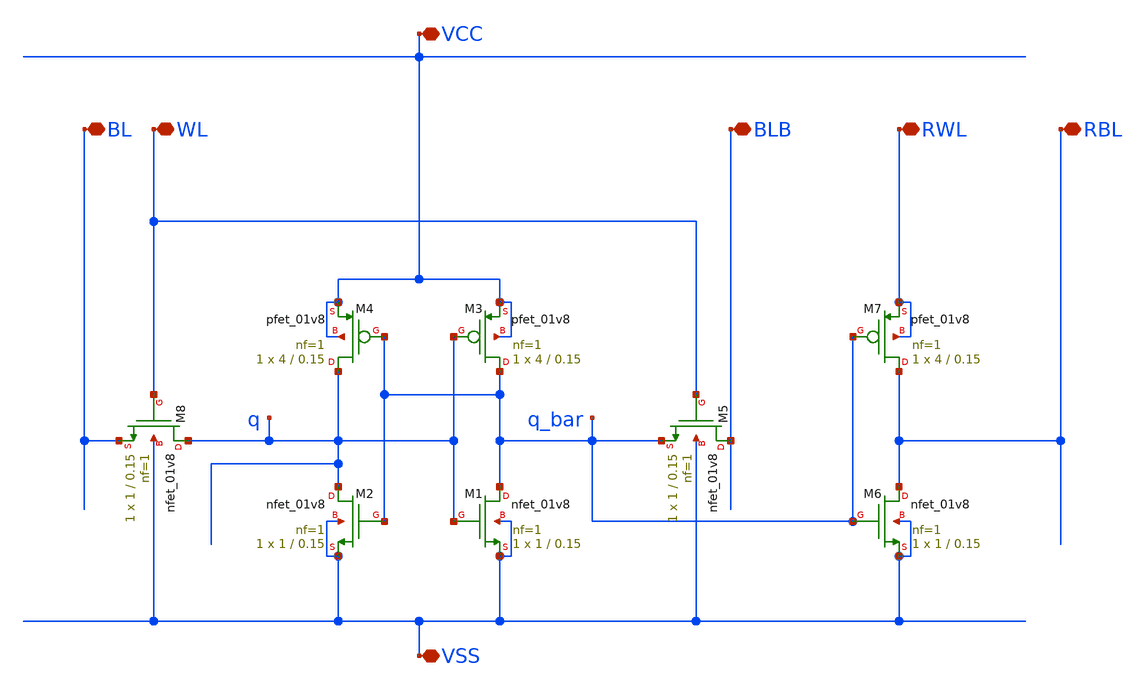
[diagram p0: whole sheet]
** sch_path: 8T_sram_cell2.sch
**.subckt 8T_sram_cell2 VCC BLB WL BL VSS RBL RWL
*.iopin VCC
*.iopin BLB
*.iopin WL
*.iopin BL
*.iopin VSS
*.iopin RBL
*.iopin RWL
XM1 q_bar q VSS VSS sky130_fd_pr__nfet_01v8 L=0.15 W=1 nf=1 ad='int((1 + 1)/2) * 1 / 1 * 0.29' as='int((1 + 2)/2) * 1 / 1 * 0.29'
+ pd='2*int((1 + 1)/2) * (1 / 1 + 0.29)' ps='2*int((1 + 2)/2) * (1 / 1 + 0.29)' nrd='0.29 / 1 ' nrs='0.29 / 1 '
+ sa=0 sb=0 sd=0 mult=1 m=1
XM2 q q_bar VSS VSS sky130_fd_pr__nfet_01v8 L=0.15 W=1 nf=1 ad='int((1 + 1)/2) * 1 / 1 * 0.29' as='int((1 + 2)/2) * 1 / 1 * 0.29'
+ pd='2*int((1 + 1)/2) * (1 / 1 + 0.29)' ps='2*int((1 + 2)/2) * (1 / 1 + 0.29)' nrd='0.29 / 1 ' nrs='0.29 / 1 '
+ sa=0 sb=0 sd=0 mult=1 m=1
XM3 q_bar q VCC VCC sky130_fd_pr__pfet_01v8 L=0.15 W=4 nf=1 ad='int((1 + 1)/2) * 4 / 1 * 0.29' as='int((1 + 2)/2) * 4 / 1 * 0.29'
+ pd='2*int((1 + 1)/2) * (4 / 1 + 0.29)' ps='2*int((1 + 2)/2) * (4 / 1 + 0.29)' nrd='0.29 / 4 ' nrs='0.29 / 4 '
+ sa=0 sb=0 sd=0 mult=1 m=1
XM4 q q_bar VCC VCC sky130_fd_pr__pfet_01v8 L=0.15 W=4 nf=1 ad='int((1 + 1)/2) * 4 / 1 * 0.29' as='int((1 + 2)/2) * 4 / 1 * 0.29'
+ pd='2*int((1 + 1)/2) * (4 / 1 + 0.29)' ps='2*int((1 + 2)/2) * (4 / 1 + 0.29)' nrd='0.29 / 4 ' nrs='0.29 / 4 '
+ sa=0 sb=0 sd=0 mult=1 m=1
XM5 BLB WL q_bar VSS sky130_fd_pr__nfet_01v8 L=0.15 W=1 nf=1 ad='int((1 + 1)/2) * 1 / 1 * 0.29' as='int((1 + 2)/2) * 1 / 1 * 0.29'
+ pd='2*int((1 + 1)/2) * (1 / 1 + 0.29)' ps='2*int((1 + 2)/2) * (1 / 1 + 0.29)' nrd='0.29 / 1 ' nrs='0.29 / 1 '
+ sa=0 sb=0 sd=0 mult=1 m=1
XM8 q WL BL VSS sky130_fd_pr__nfet_01v8 L=0.15 W=1 nf=1 ad='int((1 + 1)/2) * 1 / 1 * 0.29' as='int((1 + 2)/2) * 1 / 1 * 0.29'
+ pd='2*int((1 + 1)/2) * (1 / 1 + 0.29)' ps='2*int((1 + 2)/2) * (1 / 1 + 0.29)' nrd='0.29 / 1 ' nrs='0.29 / 1 '
+ sa=0 sb=0 sd=0 mult=1 m=1
XM6 RBL q_bar VSS VSS sky130_fd_pr__nfet_01v8 L=0.15 W=1 nf=1 ad='int((1 + 1)/2) * 1 / 1 * 0.29' as='int((1 + 2)/2) * 1 / 1 * 0.29'
+ pd='2*int((1 + 1)/2) * (1 / 1 + 0.29)' ps='2*int((1 + 2)/2) * (1 / 1 + 0.29)' nrd='0.29 / 1 ' nrs='0.29 / 1 '
+ sa=0 sb=0 sd=0 mult=1 m=1
XM7 RBL q_bar RWL RWL sky130_fd_pr__pfet_01v8 L=0.15 W=4 nf=1 ad='int((1 + 1)/2) * 4 / 1 * 0.29' as='int((1 + 2)/2) * 4 / 1 * 0.29'
+ pd='2*int((1 + 1)/2) * (4 / 1 + 0.29)' ps='2*int((1 + 2)/2) * (4 / 1 + 0.29)' nrd='0.29 / 4 ' nrs='0.29 / 4 '
+ sa=0 sb=0 sd=0 mult=1 m=1
**.ends
.end
